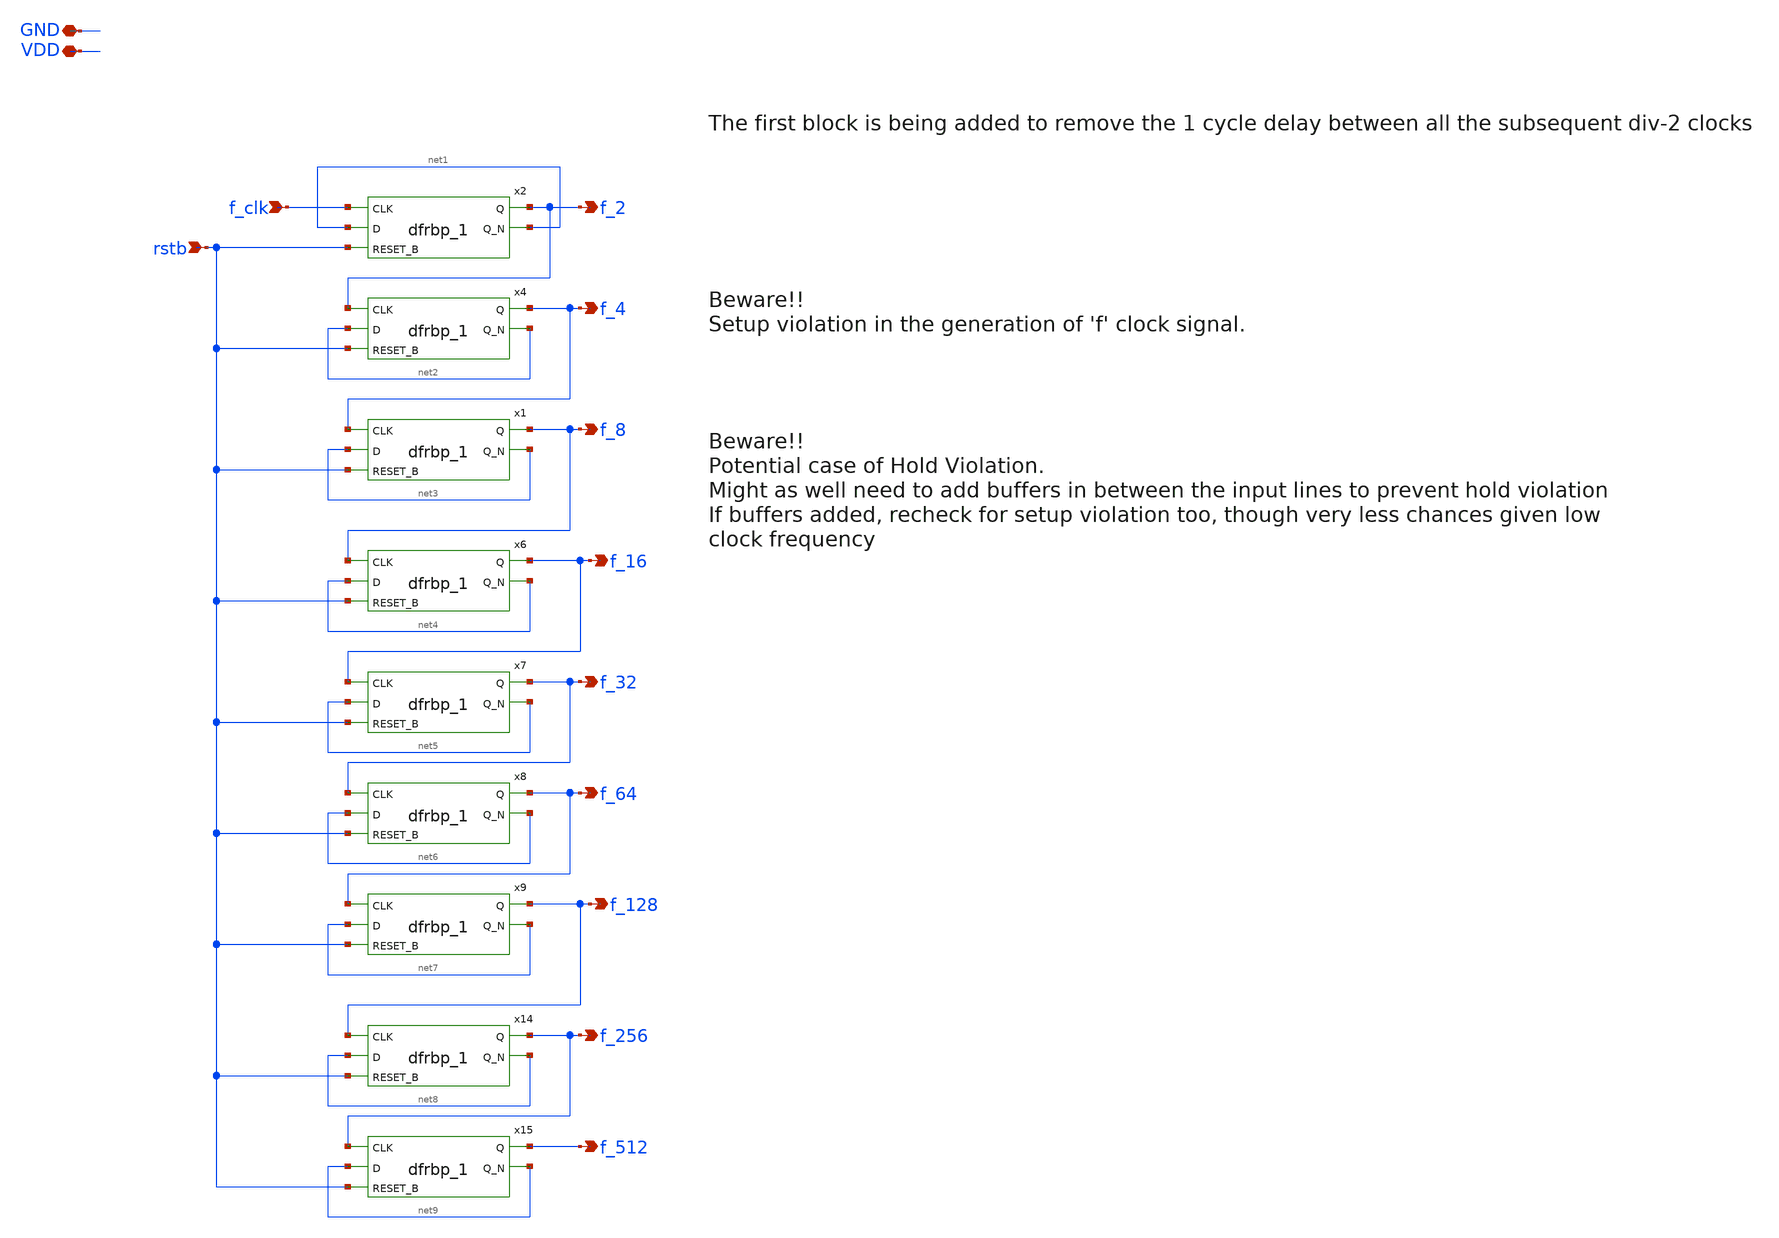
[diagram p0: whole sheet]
** sch_path: xschem/clk_tree/clk_tree.sch
**.subckt clk_tree rstb VDD GND f_2 f_4 f_8 f_16 f_32 f_64 f_128 f_256 f_512 f_clk
*.ipin rstb
*.iopin VDD
*.iopin GND
*.opin f_2
*.opin f_4
*.opin f_8
*.opin f_16
*.opin f_32
*.opin f_64
*.opin f_128
*.opin f_256
*.opin f_512
*.ipin f_clk
x2 f_clk net1 rstb gnd gnd vdd vdd f_2 net1 sky130_fd_sc_lp__dfrbp_1
x4 f_2 net2 rstb gnd gnd vdd vdd f_4 net2 sky130_fd_sc_lp__dfrbp_1
x1 f_4 net3 rstb gnd gnd vdd vdd f_8 net3 sky130_fd_sc_lp__dfrbp_1
x6 f_8 net4 rstb gnd gnd vdd vdd f_16 net4 sky130_fd_sc_lp__dfrbp_1
x7 f_16 net5 rstb gnd gnd vdd vdd f_32 net5 sky130_fd_sc_lp__dfrbp_1
x8 f_32 net6 rstb gnd gnd vdd vdd f_64 net6 sky130_fd_sc_lp__dfrbp_1
x9 f_64 net7 rstb gnd gnd vdd vdd f_128 net7 sky130_fd_sc_lp__dfrbp_1
x14 f_128 net8 rstb gnd gnd vdd vdd f_256 net8 sky130_fd_sc_lp__dfrbp_1
x15 f_256 net9 rstb gnd gnd vdd vdd f_512 net9 sky130_fd_sc_lp__dfrbp_1
**.ends
.end
